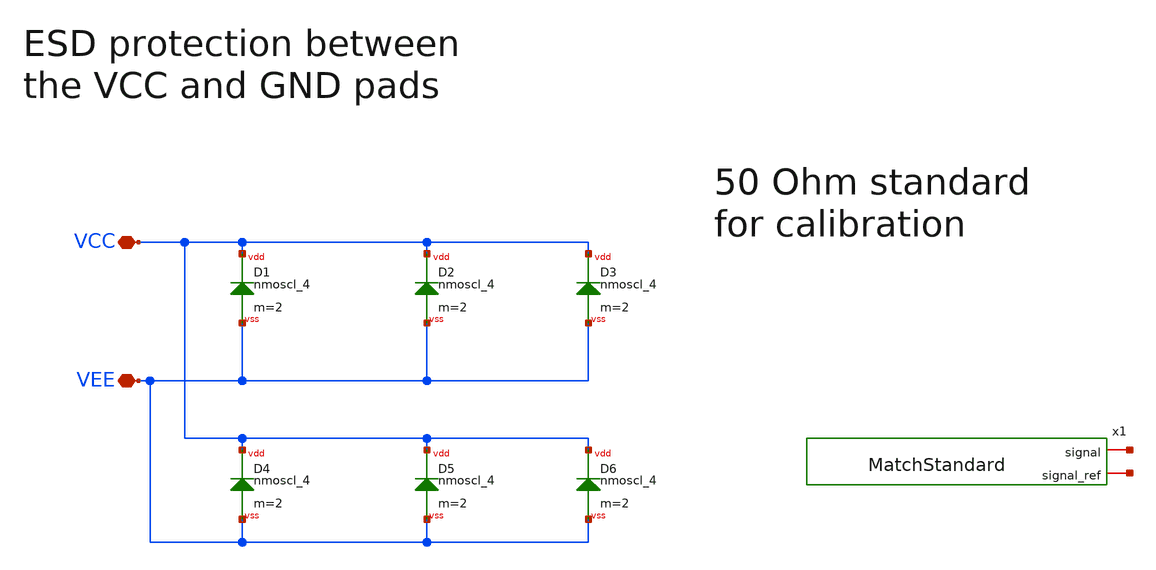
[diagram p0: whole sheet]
** sch_path: LNA0379-main/schematic/xschem/PadRing.sch
**.subckt PadRing VCC VEE
*.iopin VCC
*.iopin VEE
XD1 VCC VEE nmoscl_4 m=2
XD2 VCC VEE nmoscl_4 m=2
XD3 VCC VEE nmoscl_4 m=2
XD4 VCC VEE nmoscl_4 m=2
XD5 VCC VEE nmoscl_4 m=2
XD6 VCC VEE nmoscl_4 m=2
x1 net1 net2 MatchStandard
**.ends

* expanding   symbol:  MatchStandard.sym # of pins=2
** sym_path: LNA0379-main/schematic/xschem/MatchStandard.sym
** sch_path: LNA0379-main/schematic/xschem/MatchStandard.sch
.subckt MatchStandard signal signal_ref
*.iopin signal
*.iopin signal_ref
x1 signal signal_ref MatchResistorArray
x2 signal signal_ref MatchResistorArray
.ends


* expanding   symbol:  MatchResistorArray.sym # of pins=2
** sym_path: LNA0379-main/schematic/xschem/MatchResistorArray.sym
** sch_path: LNA0379-main/schematic/xschem/MatchResistorArray.sch
.subckt MatchResistorArray p1 p2
*.iopin p1
*.iopin p2
XR1 p1 p2 sub! rppd w=10e-6 l=19e-6 m=5 b=0 mm_ok=1
XR2 net1 net2 sub! rppd w=10e-6 l=19e-6 m=1 b=0 mm_ok=1
XR3 net3 net4 sub! rppd w=10e-6 l=19e-6 m=1 b=0 mm_ok=1
* noconn #net1
* noconn #net2
* noconn #net4
* noconn #net3
.ends

.end
